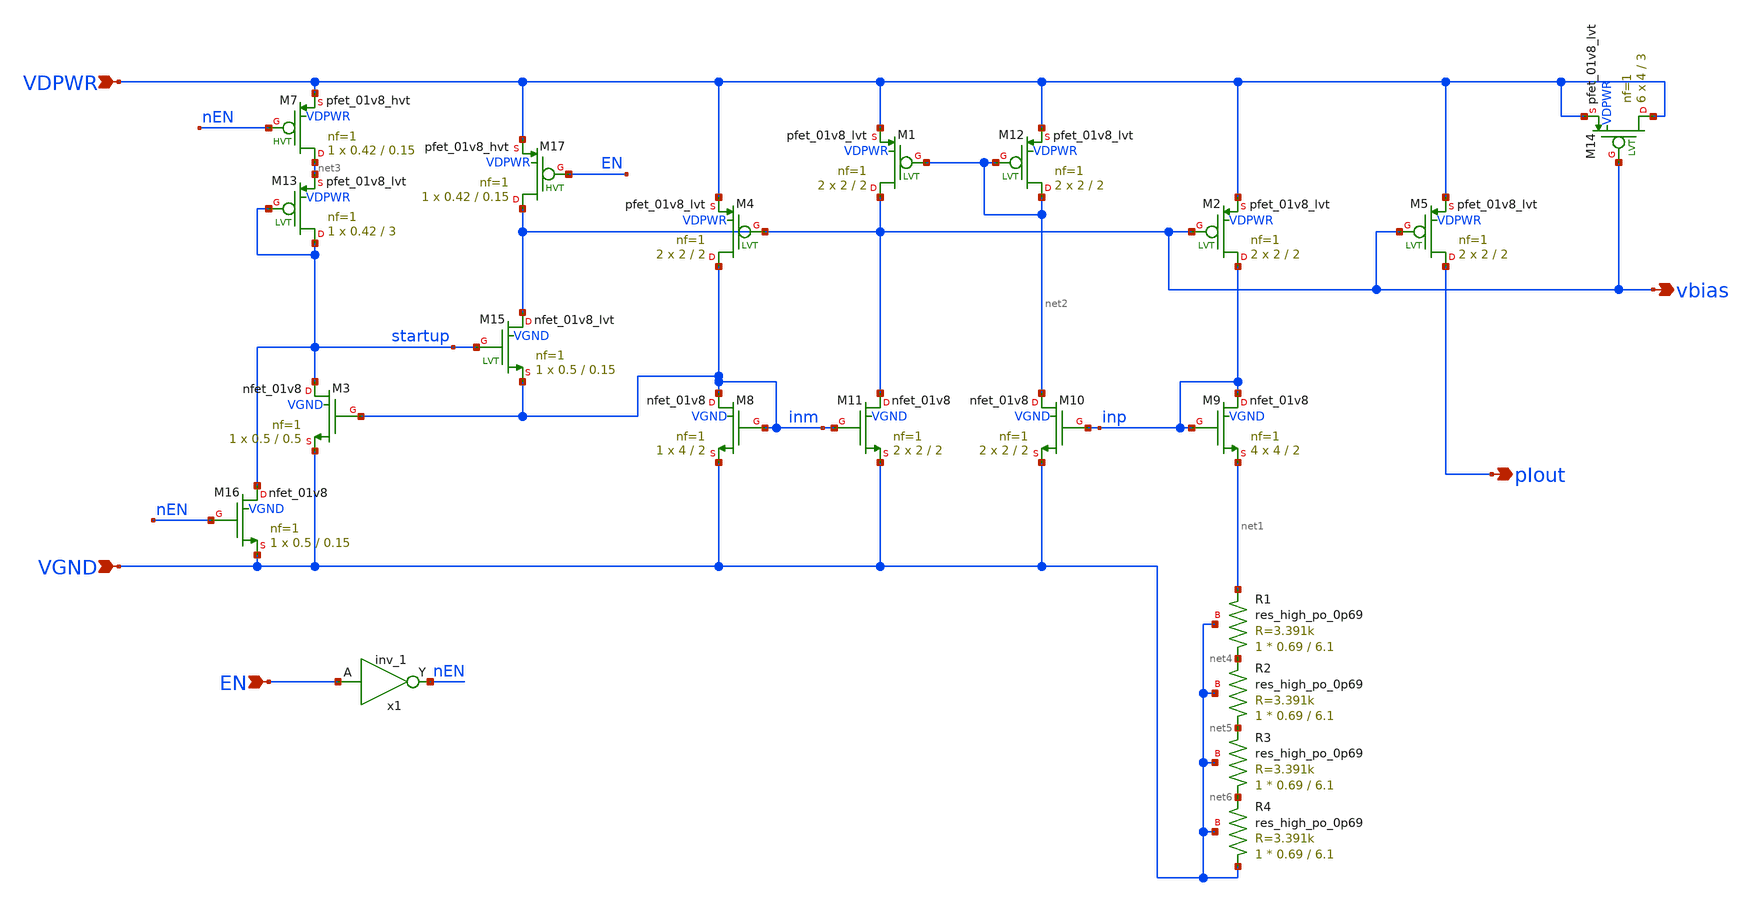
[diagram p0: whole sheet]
** sch_path: xschem/bias.sch
**.subckt bias EN pIout VGND VDPWR vbias
*.ipin EN
*.opin pIout
*.ipin VGND
*.ipin VDPWR
*.opin vbias
XM4 inm vbias VDPWR VDPWR sky130_fd_pr__pfet_01v8_lvt L=2 W=2 nf=1 ad='int((1 + 1)/2) * 2 / 1 * 0.29'
+ as='int((1 + 2)/2) * 2 / 1 * 0.29' pd='2*int((1 + 1)/2) * (2 / 1 + 0.29)' ps='2*int((1 + 2)/2) * (2 / 1 + 0.29)'
+ nrd='0.29 / 2 ' nrs='0.29 / 2 ' sa=0 sb=0 sd=0 mult=2 m=2
XM2 inp vbias VDPWR VDPWR sky130_fd_pr__pfet_01v8_lvt L=2 W=2 nf=1 ad='int((1 + 1)/2) * 2 / 1 * 0.29'
+ as='int((1 + 2)/2) * 2 / 1 * 0.29' pd='2*int((1 + 1)/2) * (2 / 1 + 0.29)' ps='2*int((1 + 2)/2) * (2 / 1 + 0.29)'
+ nrd='0.29 / 2 ' nrs='0.29 / 2 ' sa=0 sb=0 sd=0 mult=2 m=2
XM5 pIout vbias VDPWR VDPWR sky130_fd_pr__pfet_01v8_lvt L=2 W=2 nf=1 ad='int((1 + 1)/2) * 2 / 1 * 0.29'
+ as='int((1 + 2)/2) * 2 / 1 * 0.29' pd='2*int((1 + 1)/2) * (2 / 1 + 0.29)' ps='2*int((1 + 2)/2) * (2 / 1 + 0.29)'
+ nrd='0.29 / 2 ' nrs='0.29 / 2 ' sa=0 sb=0 sd=0 mult=2 m=2
XM8 inm inm VGND VGND sky130_fd_pr__nfet_01v8 L=2 W=4 nf=1 ad='int((1 + 1)/2) * 4 / 1 * 0.29' as='int((1 + 2)/2) * 4 / 1 * 0.29'
+ pd='2*int((1 + 1)/2) * (4 / 1 + 0.29)' ps='2*int((1 + 2)/2) * (4 / 1 + 0.29)' nrd='0.29 / 4 ' nrs='0.29 / 4 '
+ sa=0 sb=0 sd=0 mult=1 m=1
XM9 inp inp net1 VGND sky130_fd_pr__nfet_01v8 L=2 W=4 nf=1 ad='int((1 + 1)/2) * 4 / 1 * 0.29' as='int((1 + 2)/2) * 4 / 1 * 0.29'
+ pd='2*int((1 + 1)/2) * (4 / 1 + 0.29)' ps='2*int((1 + 2)/2) * (4 / 1 + 0.29)' nrd='0.29 / 4 ' nrs='0.29 / 4 '
+ sa=0 sb=0 sd=0 mult=4 m=4
XM10 net2 inp VGND VGND sky130_fd_pr__nfet_01v8 L=2 W=2 nf=1 ad='int((1 + 1)/2) * 2 / 1 * 0.29' as='int((1 + 2)/2) * 2 / 1 * 0.29'
+ pd='2*int((1 + 1)/2) * (2 / 1 + 0.29)' ps='2*int((1 + 2)/2) * (2 / 1 + 0.29)' nrd='0.29 / 2 ' nrs='0.29 / 2 '
+ sa=0 sb=0 sd=0 mult=2 m=2
XM11 vbias inm VGND VGND sky130_fd_pr__nfet_01v8 L=2 W=2 nf=1 ad='int((1 + 1)/2) * 2 / 1 * 0.29' as='int((1 + 2)/2) * 2 / 1 * 0.29'
+ pd='2*int((1 + 1)/2) * (2 / 1 + 0.29)' ps='2*int((1 + 2)/2) * (2 / 1 + 0.29)' nrd='0.29 / 2 ' nrs='0.29 / 2 '
+ sa=0 sb=0 sd=0 mult=2 m=2
XM15 vbias startup inm VGND sky130_fd_pr__nfet_01v8_lvt L=0.15 W=0.5 nf=1 ad='int((1 + 1)/2) * 0.5 / 1 * 0.29'
+ as='int((1 + 2)/2) * 0.5 / 1 * 0.29' pd='2*int((1 + 1)/2) * (0.5 / 1 + 0.29)' ps='2*int((1 + 2)/2) * (0.5 / 1 + 0.29)'
+ nrd='0.29 / 0.5 ' nrs='0.29 / 0.5 ' sa=0 sb=0 sd=0 mult=1 m=1
XM3 startup inm VGND VGND sky130_fd_pr__nfet_01v8 L=0.5 W=0.5 nf=1 ad='int((1 + 1)/2) * 0.5 / 1 * 0.29'
+ as='int((1 + 2)/2) * 0.5 / 1 * 0.29' pd='2*int((1 + 1)/2) * (0.5 / 1 + 0.29)' ps='2*int((1 + 2)/2) * (0.5 / 1 + 0.29)'
+ nrd='0.29 / 0.5 ' nrs='0.29 / 0.5 ' sa=0 sb=0 sd=0 mult=1 m=1
XR1 net4 net1 VGND sky130_fd_pr__res_high_po_0p69 L=6.1 mult=1 m=1
XR2 net5 net4 VGND sky130_fd_pr__res_high_po_0p69 L=6.1 mult=1 m=1
XR3 net6 net5 VGND sky130_fd_pr__res_high_po_0p69 L=6.1 mult=1 m=1
XR4 VGND net6 VGND sky130_fd_pr__res_high_po_0p69 L=6.1 mult=1 m=1
XM1 vbias net2 VDPWR VDPWR sky130_fd_pr__pfet_01v8_lvt L=2 W=2 nf=1 ad='int((1 + 1)/2) * 2 / 1 * 0.29'
+ as='int((1 + 2)/2) * 2 / 1 * 0.29' pd='2*int((1 + 1)/2) * (2 / 1 + 0.29)' ps='2*int((1 + 2)/2) * (2 / 1 + 0.29)'
+ nrd='0.29 / 2 ' nrs='0.29 / 2 ' sa=0 sb=0 sd=0 mult=2 m=2
XM12 net2 net2 VDPWR VDPWR sky130_fd_pr__pfet_01v8_lvt L=2 W=2 nf=1 ad='int((1 + 1)/2) * 2 / 1 * 0.29'
+ as='int((1 + 2)/2) * 2 / 1 * 0.29' pd='2*int((1 + 1)/2) * (2 / 1 + 0.29)' ps='2*int((1 + 2)/2) * (2 / 1 + 0.29)'
+ nrd='0.29 / 2 ' nrs='0.29 / 2 ' sa=0 sb=0 sd=0 mult=2 m=2
XM13 startup startup net3 VDPWR sky130_fd_pr__pfet_01v8_lvt L=3 W=0.42 nf=1 ad='int((1 + 1)/2) * 0.42 / 1 * 0.29'
+ as='int((1 + 2)/2) * 0.42 / 1 * 0.29' pd='2*int((1 + 1)/2) * (0.42 / 1 + 0.29)' ps='2*int((1 + 2)/2) * (0.42 / 1 + 0.29)'
+ nrd='0.29 / 0.42 ' nrs='0.29 / 0.42 ' sa=0 sb=0 sd=0 mult=1 m=1
XM16 startup nEN VGND VGND sky130_fd_pr__nfet_01v8 L=0.15 W=0.5 nf=1 ad='int((1 + 1)/2) * 0.5 / 1 * 0.29'
+ as='int((1 + 2)/2) * 0.5 / 1 * 0.29' pd='2*int((1 + 1)/2) * (0.5 / 1 + 0.29)' ps='2*int((1 + 2)/2) * (0.5 / 1 + 0.29)'
+ nrd='0.29 / 0.5 ' nrs='0.29 / 0.5 ' sa=0 sb=0 sd=0 mult=1 m=1
XM17 vbias EN VDPWR VDPWR sky130_fd_pr__pfet_01v8_hvt L=0.15 W=0.42 nf=1 ad='int((1 + 1)/2) * 0.42 / 1 * 0.29'
+ as='int((1 + 2)/2) * 0.42 / 1 * 0.29' pd='2*int((1 + 1)/2) * (0.42 / 1 + 0.29)' ps='2*int((1 + 2)/2) * (0.42 / 1 + 0.29)'
+ nrd='0.29 / 0.42 ' nrs='0.29 / 0.42 ' sa=0 sb=0 sd=0 mult=1 m=1
XM7 net3 nEN VDPWR VDPWR sky130_fd_pr__pfet_01v8_hvt L=0.15 W=0.42 nf=1 ad='int((1 + 1)/2) * 0.42 / 1 * 0.29'
+ as='int((1 + 2)/2) * 0.42 / 1 * 0.29' pd='2*int((1 + 1)/2) * (0.42 / 1 + 0.29)' ps='2*int((1 + 2)/2) * (0.42 / 1 + 0.29)'
+ nrd='0.29 / 0.42 ' nrs='0.29 / 0.42 ' sa=0 sb=0 sd=0 mult=1 m=1
XM14 VDPWR vbias VDPWR VDPWR sky130_fd_pr__pfet_01v8_lvt L=3 W=4 nf=1 ad='int((1 + 1)/2) * 4 / 1 * 0.29'
+ as='int((1 + 2)/2) * 4 / 1 * 0.29' pd='2*int((1 + 1)/2) * (4 / 1 + 0.29)' ps='2*int((1 + 2)/2) * (4 / 1 + 0.29)'
+ nrd='0.29 / 4 ' nrs='0.29 / 4 ' sa=0 sb=0 sd=0 mult=6 m=6
x1 EN VGND VGND VDPWR VDPWR nEN sky130_fd_sc_hd__inv_1
**.ends
.end
